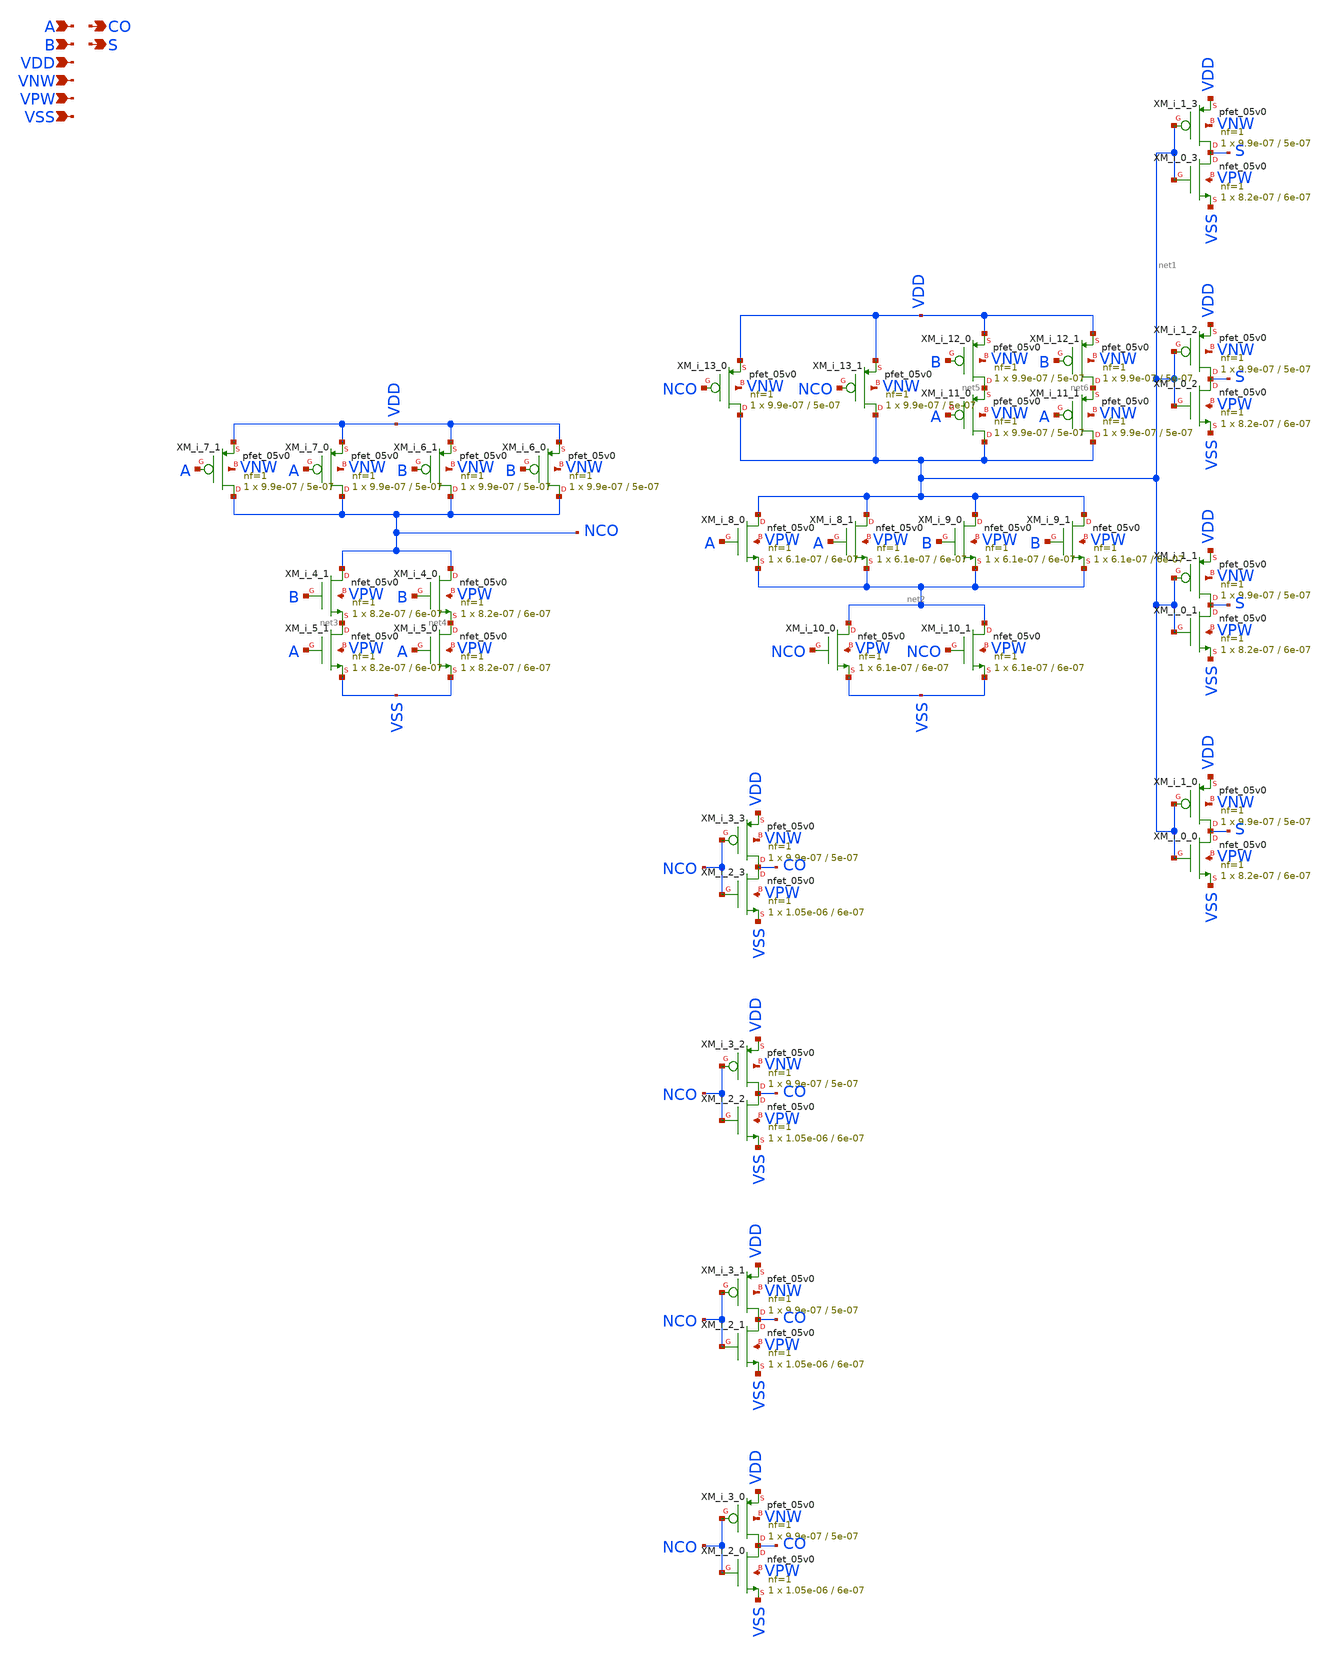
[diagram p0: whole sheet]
** sch_path: schematics/addh/gf180mcu_fd_sc_mcu7t5v0__addh_4.sch
**.subckt gf180mcu_fd_sc_mcu7t5v0__addh_4 A B CO S VDD VNW VPW VSS
*.ipin A
*.ipin B
*.opin CO
*.opin S
*.ipin VDD
*.ipin VNW
*.ipin VPW
*.ipin VSS
XM_i_7_1 NCO A VDD VNW pfet_05v0 L=5e-07 W=9.9e-07 nf=1 ad='int((nf+1)/2) * W/nf * 0.18u' as='int((nf+2)/2) * W/nf * 0.18u'
+ pd='2*int((nf+1)/2) * (W/nf + 0.18u)' ps='2*int((nf+2)/2) * (W/nf + 0.18u)' nrd='0.18u / W' nrs='0.18u / W'
+ sa=0 sb=0 sd=0 m=1 par=1
XM_i_7_0 NCO A VDD VNW pfet_05v0 L=5e-07 W=9.9e-07 nf=1 ad='int((nf+1)/2) * W/nf * 0.18u' as='int((nf+2)/2) * W/nf * 0.18u'
+ pd='2*int((nf+1)/2) * (W/nf + 0.18u)' ps='2*int((nf+2)/2) * (W/nf + 0.18u)' nrd='0.18u / W' nrs='0.18u / W'
+ sa=0 sb=0 sd=0 m=1 par=1
XM_i_6_1 NCO B VDD VNW pfet_05v0 L=5e-07 W=9.9e-07 nf=1 ad='int((nf+1)/2) * W/nf * 0.18u' as='int((nf+2)/2) * W/nf * 0.18u'
+ pd='2*int((nf+1)/2) * (W/nf + 0.18u)' ps='2*int((nf+2)/2) * (W/nf + 0.18u)' nrd='0.18u / W' nrs='0.18u / W'
+ sa=0 sb=0 sd=0 m=1 par=1
XM_i_6_0 NCO B VDD VNW pfet_05v0 L=5e-07 W=9.9e-07 nf=1 ad='int((nf+1)/2) * W/nf * 0.18u' as='int((nf+2)/2) * W/nf * 0.18u'
+ pd='2*int((nf+1)/2) * (W/nf + 0.18u)' ps='2*int((nf+2)/2) * (W/nf + 0.18u)' nrd='0.18u / W' nrs='0.18u / W'
+ sa=0 sb=0 sd=0 m=1 par=1
XM_i_4_1 NCO B net3 VPW nfet_05v0 L=6e-07 W=8.2e-07 nf=1 ad='int((nf+1)/2) * W/nf * 0.18u' as='int((nf+2)/2) * W/nf * 0.18u'
+ pd='2*int((nf+1)/2) * (W/nf + 0.18u)' ps='2*int((nf+2)/2) * (W/nf + 0.18u)' nrd='0.18u / W' nrs='0.18u / W'
+ sa=0 sb=0 sd=0 m=1
XM_i_5_1 net3 A VSS VPW nfet_05v0 L=6e-07 W=8.2e-07 nf=1 ad='int((nf+1)/2) * W/nf * 0.18u' as='int((nf+2)/2) * W/nf * 0.18u'
+ pd='2*int((nf+1)/2) * (W/nf + 0.18u)' ps='2*int((nf+2)/2) * (W/nf + 0.18u)' nrd='0.18u / W' nrs='0.18u / W'
+ sa=0 sb=0 sd=0 m=1
XM_i_4_0 NCO B net4 VPW nfet_05v0 L=6e-07 W=8.2e-07 nf=1 ad='int((nf+1)/2) * W/nf * 0.18u' as='int((nf+2)/2) * W/nf * 0.18u'
+ pd='2*int((nf+1)/2) * (W/nf + 0.18u)' ps='2*int((nf+2)/2) * (W/nf + 0.18u)' nrd='0.18u / W' nrs='0.18u / W'
+ sa=0 sb=0 sd=0 m=1
XM_i_5_0 net4 A VSS VPW nfet_05v0 L=6e-07 W=8.2e-07 nf=1 ad='int((nf+1)/2) * W/nf * 0.18u' as='int((nf+2)/2) * W/nf * 0.18u'
+ pd='2*int((nf+1)/2) * (W/nf + 0.18u)' ps='2*int((nf+2)/2) * (W/nf + 0.18u)' nrd='0.18u / W' nrs='0.18u / W'
+ sa=0 sb=0 sd=0 m=1
XM_i_13_0 net1 NCO VDD VNW pfet_05v0 L=5e-07 W=9.9e-07 nf=1 ad='int((nf+1)/2) * W/nf * 0.18u' as='int((nf+2)/2) * W/nf * 0.18u'
+ pd='2*int((nf+1)/2) * (W/nf + 0.18u)' ps='2*int((nf+2)/2) * (W/nf + 0.18u)' nrd='0.18u / W' nrs='0.18u / W'
+ sa=0 sb=0 sd=0 m=1 par=1
XM_i_13_1 net1 NCO VDD VNW pfet_05v0 L=5e-07 W=9.9e-07 nf=1 ad='int((nf+1)/2) * W/nf * 0.18u' as='int((nf+2)/2) * W/nf * 0.18u'
+ pd='2*int((nf+1)/2) * (W/nf + 0.18u)' ps='2*int((nf+2)/2) * (W/nf + 0.18u)' nrd='0.18u / W' nrs='0.18u / W'
+ sa=0 sb=0 sd=0 m=1 par=1
XM_i_12_0 net5 B VDD VNW pfet_05v0 L=5e-07 W=9.9e-07 nf=1 ad='int((nf+1)/2) * W/nf * 0.18u' as='int((nf+2)/2) * W/nf * 0.18u'
+ pd='2*int((nf+1)/2) * (W/nf + 0.18u)' ps='2*int((nf+2)/2) * (W/nf + 0.18u)' nrd='0.18u / W' nrs='0.18u / W'
+ sa=0 sb=0 sd=0 m=1 par=1
XM_i_11_0 net1 A net5 VNW pfet_05v0 L=5e-07 W=9.9e-07 nf=1 ad='int((nf+1)/2) * W/nf * 0.18u' as='int((nf+2)/2) * W/nf * 0.18u'
+ pd='2*int((nf+1)/2) * (W/nf + 0.18u)' ps='2*int((nf+2)/2) * (W/nf + 0.18u)' nrd='0.18u / W' nrs='0.18u / W'
+ sa=0 sb=0 sd=0 m=1 par=1
XM_i_12_1 net6 B VDD VNW pfet_05v0 L=5e-07 W=9.9e-07 nf=1 ad='int((nf+1)/2) * W/nf * 0.18u' as='int((nf+2)/2) * W/nf * 0.18u'
+ pd='2*int((nf+1)/2) * (W/nf + 0.18u)' ps='2*int((nf+2)/2) * (W/nf + 0.18u)' nrd='0.18u / W' nrs='0.18u / W'
+ sa=0 sb=0 sd=0 m=1 par=1
XM_i_11_1 net1 A net6 VNW pfet_05v0 L=5e-07 W=9.9e-07 nf=1 ad='int((nf+1)/2) * W/nf * 0.18u' as='int((nf+2)/2) * W/nf * 0.18u'
+ pd='2*int((nf+1)/2) * (W/nf + 0.18u)' ps='2*int((nf+2)/2) * (W/nf + 0.18u)' nrd='0.18u / W' nrs='0.18u / W'
+ sa=0 sb=0 sd=0 m=1 par=1
XM_i_8_0 net1 A net2 VPW nfet_05v0 L=6e-07 W=6.1e-07 nf=1 ad='int((nf+1)/2) * W/nf * 0.18u' as='int((nf+2)/2) * W/nf * 0.18u'
+ pd='2*int((nf+1)/2) * (W/nf + 0.18u)' ps='2*int((nf+2)/2) * (W/nf + 0.18u)' nrd='0.18u / W' nrs='0.18u / W'
+ sa=0 sb=0 sd=0 m=1
XM_i_8_1 net1 A net2 VPW nfet_05v0 L=6e-07 W=6.1e-07 nf=1 ad='int((nf+1)/2) * W/nf * 0.18u' as='int((nf+2)/2) * W/nf * 0.18u'
+ pd='2*int((nf+1)/2) * (W/nf + 0.18u)' ps='2*int((nf+2)/2) * (W/nf + 0.18u)' nrd='0.18u / W' nrs='0.18u / W'
+ sa=0 sb=0 sd=0 m=1
XM_i_9_0 net1 B net2 VPW nfet_05v0 L=6e-07 W=6.1e-07 nf=1 ad='int((nf+1)/2) * W/nf * 0.18u' as='int((nf+2)/2) * W/nf * 0.18u'
+ pd='2*int((nf+1)/2) * (W/nf + 0.18u)' ps='2*int((nf+2)/2) * (W/nf + 0.18u)' nrd='0.18u / W' nrs='0.18u / W'
+ sa=0 sb=0 sd=0 m=1
XM_i_9_1 net1 B net2 VPW nfet_05v0 L=6e-07 W=6.1e-07 nf=1 ad='int((nf+1)/2) * W/nf * 0.18u' as='int((nf+2)/2) * W/nf * 0.18u'
+ pd='2*int((nf+1)/2) * (W/nf + 0.18u)' ps='2*int((nf+2)/2) * (W/nf + 0.18u)' nrd='0.18u / W' nrs='0.18u / W'
+ sa=0 sb=0 sd=0 m=1
XM_i_10_0 net2 NCO VSS VPW nfet_05v0 L=6e-07 W=6.1e-07 nf=1 ad='int((nf+1)/2) * W/nf * 0.18u' as='int((nf+2)/2) * W/nf * 0.18u'
+ pd='2*int((nf+1)/2) * (W/nf + 0.18u)' ps='2*int((nf+2)/2) * (W/nf + 0.18u)' nrd='0.18u / W' nrs='0.18u / W'
+ sa=0 sb=0 sd=0 m=1
XM_i_10_1 net2 NCO VSS VPW nfet_05v0 L=6e-07 W=6.1e-07 nf=1 ad='int((nf+1)/2) * W/nf * 0.18u' as='int((nf+2)/2) * W/nf * 0.18u'
+ pd='2*int((nf+1)/2) * (W/nf + 0.18u)' ps='2*int((nf+2)/2) * (W/nf + 0.18u)' nrd='0.18u / W' nrs='0.18u / W'
+ sa=0 sb=0 sd=0 m=1
XM_i_3_3 CO NCO VDD VNW pfet_05v0 L=5e-07 W=9.9e-07 nf=1 ad='int((nf+1)/2) * W/nf * 0.18u' as='int((nf+2)/2) * W/nf * 0.18u'
+ pd='2*int((nf+1)/2) * (W/nf + 0.18u)' ps='2*int((nf+2)/2) * (W/nf + 0.18u)' nrd='0.18u / W' nrs='0.18u / W'
+ sa=0 sb=0 sd=0 m=1 par=1
XM_i_2_3 CO NCO VSS VPW nfet_05v0 L=6e-07 W=1.05e-06 nf=1 ad='int((nf+1)/2) * W/nf * 0.18u' as='int((nf+2)/2) * W/nf * 0.18u'
+ pd='2*int((nf+1)/2) * (W/nf + 0.18u)' ps='2*int((nf+2)/2) * (W/nf + 0.18u)' nrd='0.18u / W' nrs='0.18u / W'
+ sa=0 sb=0 sd=0 m=1
XM_i_3_2 CO NCO VDD VNW pfet_05v0 L=5e-07 W=9.9e-07 nf=1 ad='int((nf+1)/2) * W/nf * 0.18u' as='int((nf+2)/2) * W/nf * 0.18u'
+ pd='2*int((nf+1)/2) * (W/nf + 0.18u)' ps='2*int((nf+2)/2) * (W/nf + 0.18u)' nrd='0.18u / W' nrs='0.18u / W'
+ sa=0 sb=0 sd=0 m=1 par=1
XM_i_2_2 CO NCO VSS VPW nfet_05v0 L=6e-07 W=1.05e-06 nf=1 ad='int((nf+1)/2) * W/nf * 0.18u' as='int((nf+2)/2) * W/nf * 0.18u'
+ pd='2*int((nf+1)/2) * (W/nf + 0.18u)' ps='2*int((nf+2)/2) * (W/nf + 0.18u)' nrd='0.18u / W' nrs='0.18u / W'
+ sa=0 sb=0 sd=0 m=1
XM_i_3_1 CO NCO VDD VNW pfet_05v0 L=5e-07 W=9.9e-07 nf=1 ad='int((nf+1)/2) * W/nf * 0.18u' as='int((nf+2)/2) * W/nf * 0.18u'
+ pd='2*int((nf+1)/2) * (W/nf + 0.18u)' ps='2*int((nf+2)/2) * (W/nf + 0.18u)' nrd='0.18u / W' nrs='0.18u / W'
+ sa=0 sb=0 sd=0 m=1 par=1
XM_i_2_1 CO NCO VSS VPW nfet_05v0 L=6e-07 W=1.05e-06 nf=1 ad='int((nf+1)/2) * W/nf * 0.18u' as='int((nf+2)/2) * W/nf * 0.18u'
+ pd='2*int((nf+1)/2) * (W/nf + 0.18u)' ps='2*int((nf+2)/2) * (W/nf + 0.18u)' nrd='0.18u / W' nrs='0.18u / W'
+ sa=0 sb=0 sd=0 m=1
XM_i_3_0 CO NCO VDD VNW pfet_05v0 L=5e-07 W=9.9e-07 nf=1 ad='int((nf+1)/2) * W/nf * 0.18u' as='int((nf+2)/2) * W/nf * 0.18u'
+ pd='2*int((nf+1)/2) * (W/nf + 0.18u)' ps='2*int((nf+2)/2) * (W/nf + 0.18u)' nrd='0.18u / W' nrs='0.18u / W'
+ sa=0 sb=0 sd=0 m=1 par=1
XM_i_2_0 CO NCO VSS VPW nfet_05v0 L=6e-07 W=1.05e-06 nf=1 ad='int((nf+1)/2) * W/nf * 0.18u' as='int((nf+2)/2) * W/nf * 0.18u'
+ pd='2*int((nf+1)/2) * (W/nf + 0.18u)' ps='2*int((nf+2)/2) * (W/nf + 0.18u)' nrd='0.18u / W' nrs='0.18u / W'
+ sa=0 sb=0 sd=0 m=1
XM_i_1_3 S net1 VDD VNW pfet_05v0 L=5e-07 W=9.9e-07 nf=1 ad='int((nf+1)/2) * W/nf * 0.18u' as='int((nf+2)/2) * W/nf * 0.18u'
+ pd='2*int((nf+1)/2) * (W/nf + 0.18u)' ps='2*int((nf+2)/2) * (W/nf + 0.18u)' nrd='0.18u / W' nrs='0.18u / W'
+ sa=0 sb=0 sd=0 m=1 par=1
XM_i_0_3 S net1 VSS VPW nfet_05v0 L=6e-07 W=8.2e-07 nf=1 ad='int((nf+1)/2) * W/nf * 0.18u' as='int((nf+2)/2) * W/nf * 0.18u'
+ pd='2*int((nf+1)/2) * (W/nf + 0.18u)' ps='2*int((nf+2)/2) * (W/nf + 0.18u)' nrd='0.18u / W' nrs='0.18u / W'
+ sa=0 sb=0 sd=0 m=1
XM_i_1_2 S net1 VDD VNW pfet_05v0 L=5e-07 W=9.9e-07 nf=1 ad='int((nf+1)/2) * W/nf * 0.18u' as='int((nf+2)/2) * W/nf * 0.18u'
+ pd='2*int((nf+1)/2) * (W/nf + 0.18u)' ps='2*int((nf+2)/2) * (W/nf + 0.18u)' nrd='0.18u / W' nrs='0.18u / W'
+ sa=0 sb=0 sd=0 m=1 par=1
XM_i_0_2 S net1 VSS VPW nfet_05v0 L=6e-07 W=8.2e-07 nf=1 ad='int((nf+1)/2) * W/nf * 0.18u' as='int((nf+2)/2) * W/nf * 0.18u'
+ pd='2*int((nf+1)/2) * (W/nf + 0.18u)' ps='2*int((nf+2)/2) * (W/nf + 0.18u)' nrd='0.18u / W' nrs='0.18u / W'
+ sa=0 sb=0 sd=0 m=1
XM_i_1_1 S net1 VDD VNW pfet_05v0 L=5e-07 W=9.9e-07 nf=1 ad='int((nf+1)/2) * W/nf * 0.18u' as='int((nf+2)/2) * W/nf * 0.18u'
+ pd='2*int((nf+1)/2) * (W/nf + 0.18u)' ps='2*int((nf+2)/2) * (W/nf + 0.18u)' nrd='0.18u / W' nrs='0.18u / W'
+ sa=0 sb=0 sd=0 m=1 par=1
XM_i_0_1 S net1 VSS VPW nfet_05v0 L=6e-07 W=8.2e-07 nf=1 ad='int((nf+1)/2) * W/nf * 0.18u' as='int((nf+2)/2) * W/nf * 0.18u'
+ pd='2*int((nf+1)/2) * (W/nf + 0.18u)' ps='2*int((nf+2)/2) * (W/nf + 0.18u)' nrd='0.18u / W' nrs='0.18u / W'
+ sa=0 sb=0 sd=0 m=1
XM_i_1_0 S net1 VDD VNW pfet_05v0 L=5e-07 W=9.9e-07 nf=1 ad='int((nf+1)/2) * W/nf * 0.18u' as='int((nf+2)/2) * W/nf * 0.18u'
+ pd='2*int((nf+1)/2) * (W/nf + 0.18u)' ps='2*int((nf+2)/2) * (W/nf + 0.18u)' nrd='0.18u / W' nrs='0.18u / W'
+ sa=0 sb=0 sd=0 m=1 par=1
XM_i_0_0 S net1 VSS VPW nfet_05v0 L=6e-07 W=8.2e-07 nf=1 ad='int((nf+1)/2) * W/nf * 0.18u' as='int((nf+2)/2) * W/nf * 0.18u'
+ pd='2*int((nf+1)/2) * (W/nf + 0.18u)' ps='2*int((nf+2)/2) * (W/nf + 0.18u)' nrd='0.18u / W' nrs='0.18u / W'
+ sa=0 sb=0 sd=0 m=1
**.ends
.end
